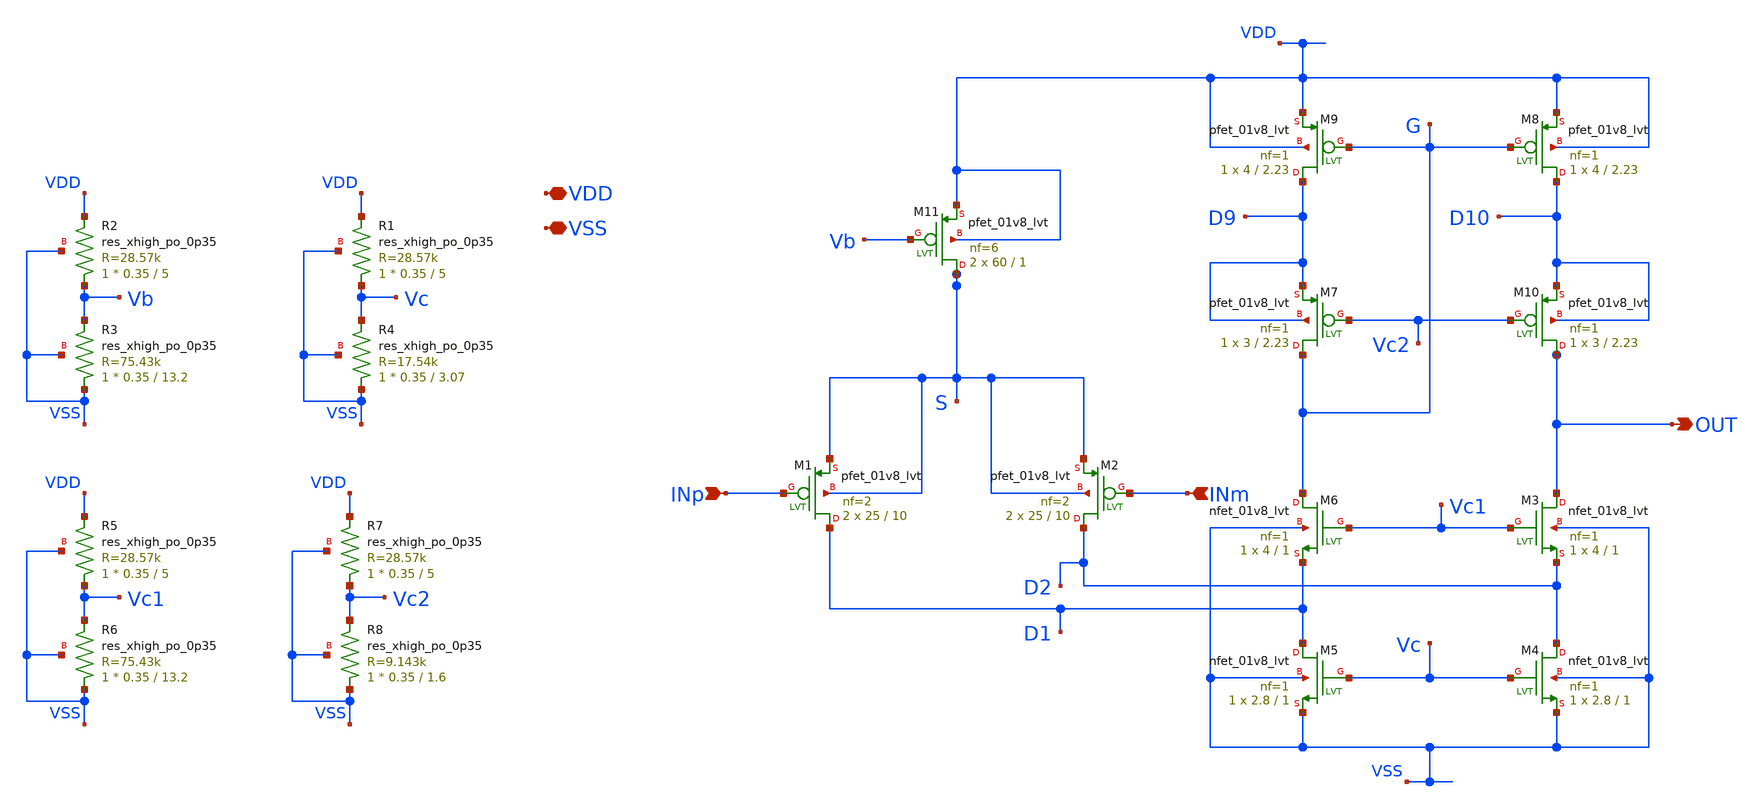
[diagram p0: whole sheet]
** sch_path: tt_um_NE567Mixer28/xschem/OFC.sch
**.subckt OFC VDD VSS INp INm OUT
*.iopin VDD
*.iopin VSS
*.ipin INp
*.ipin INm
*.opin OUT
XM11 S Vb VDD VDD sky130_fd_pr__pfet_01v8_lvt L=1 W=60 nf=6 ad='int((nf+1)/2) * W/nf * 0.29' as='int((nf+2)/2) * W/nf * 0.29'
+ pd='2*int((nf+1)/2) * (W/nf + 0.29)' ps='2*int((nf+2)/2) * (W/nf + 0.29)' nrd='0.29 / W' nrs='0.29 / W'
+ sa=0 sb=0 sd=0 mult=2 m=2
XM1 D1 INp S S sky130_fd_pr__pfet_01v8_lvt L=10 W=25 nf=2 ad='int((nf+1)/2) * W/nf * 0.29' as='int((nf+2)/2) * W/nf * 0.29'
+ pd='2*int((nf+1)/2) * (W/nf + 0.29)' ps='2*int((nf+2)/2) * (W/nf + 0.29)' nrd='0.29 / W' nrs='0.29 / W'
+ sa=0 sb=0 sd=0 mult=2 m=2
XM2 D2 INm S S sky130_fd_pr__pfet_01v8_lvt L=10 W=25 nf=2 ad='int((nf+1)/2) * W/nf * 0.29' as='int((nf+2)/2) * W/nf * 0.29'
+ pd='2*int((nf+1)/2) * (W/nf + 0.29)' ps='2*int((nf+2)/2) * (W/nf + 0.29)' nrd='0.29 / W' nrs='0.29 / W'
+ sa=0 sb=0 sd=0 mult=2 m=2
XM3 OUT Vc1 D2 VSS sky130_fd_pr__nfet_01v8_lvt L=1 W=4 nf=1 ad='int((nf+1)/2) * W/nf * 0.29' as='int((nf+2)/2) * W/nf * 0.29'
+ pd='2*int((nf+1)/2) * (W/nf + 0.29)' ps='2*int((nf+2)/2) * (W/nf + 0.29)' nrd='0.29 / W' nrs='0.29 / W'
+ sa=0 sb=0 sd=0 mult=1 m=1
XM4 D2 Vc VSS VSS sky130_fd_pr__nfet_01v8_lvt L=1 W=2.8 nf=1 ad='int((nf+1)/2) * W/nf * 0.29' as='int((nf+2)/2) * W/nf * 0.29'
+ pd='2*int((nf+1)/2) * (W/nf + 0.29)' ps='2*int((nf+2)/2) * (W/nf + 0.29)' nrd='0.29 / W' nrs='0.29 / W'
+ sa=0 sb=0 sd=0 mult=1 m=1
XM5 D1 Vc VSS VSS sky130_fd_pr__nfet_01v8_lvt L=1 W=2.8 nf=1 ad='int((nf+1)/2) * W/nf * 0.29' as='int((nf+2)/2) * W/nf * 0.29'
+ pd='2*int((nf+1)/2) * (W/nf + 0.29)' ps='2*int((nf+2)/2) * (W/nf + 0.29)' nrd='0.29 / W' nrs='0.29 / W'
+ sa=0 sb=0 sd=0 mult=1 m=1
XM6 G Vc1 D1 VSS sky130_fd_pr__nfet_01v8_lvt L=1 W=4 nf=1 ad='int((nf+1)/2) * W/nf * 0.29' as='int((nf+2)/2) * W/nf * 0.29'
+ pd='2*int((nf+1)/2) * (W/nf + 0.29)' ps='2*int((nf+2)/2) * (W/nf + 0.29)' nrd='0.29 / W' nrs='0.29 / W'
+ sa=0 sb=0 sd=0 mult=1 m=1
XM7 G Vc2 D9 D9 sky130_fd_pr__pfet_01v8_lvt L=2.23 W=3 nf=1 ad='int((nf+1)/2) * W/nf * 0.29' as='int((nf+2)/2) * W/nf * 0.29'
+ pd='2*int((nf+1)/2) * (W/nf + 0.29)' ps='2*int((nf+2)/2) * (W/nf + 0.29)' nrd='0.29 / W' nrs='0.29 / W'
+ sa=0 sb=0 sd=0 mult=1 m=1
XM9 D9 G VDD VDD sky130_fd_pr__pfet_01v8_lvt L=2.23 W=4 nf=1 ad='int((nf+1)/2) * W/nf * 0.29' as='int((nf+2)/2) * W/nf * 0.29'
+ pd='2*int((nf+1)/2) * (W/nf + 0.29)' ps='2*int((nf+2)/2) * (W/nf + 0.29)' nrd='0.29 / W' nrs='0.29 / W'
+ sa=0 sb=0 sd=0 mult=1 m=1
XM8 D10 G VDD VDD sky130_fd_pr__pfet_01v8_lvt L=2.23 W=4 nf=1 ad='int((nf+1)/2) * W/nf * 0.29' as='int((nf+2)/2) * W/nf * 0.29'
+ pd='2*int((nf+1)/2) * (W/nf + 0.29)' ps='2*int((nf+2)/2) * (W/nf + 0.29)' nrd='0.29 / W' nrs='0.29 / W'
+ sa=0 sb=0 sd=0 mult=1 m=1
XM10 OUT Vc2 D10 D10 sky130_fd_pr__pfet_01v8_lvt L=2.23 W=3 nf=1 ad='int((nf+1)/2) * W/nf * 0.29' as='int((nf+2)/2) * W/nf * 0.29'
+ pd='2*int((nf+1)/2) * (W/nf + 0.29)' ps='2*int((nf+2)/2) * (W/nf + 0.29)' nrd='0.29 / W' nrs='0.29 / W'
+ sa=0 sb=0 sd=0 mult=1 m=1
XR2 Vb VDD VSS sky130_fd_pr__res_xhigh_po_0p35 L=5 mult=1 m=1
XR3 VSS Vb VSS sky130_fd_pr__res_xhigh_po_0p35 L=13.2 mult=1 m=1
XR1 Vc VDD VSS sky130_fd_pr__res_xhigh_po_0p35 L=5 mult=1 m=1
XR4 VSS Vc VSS sky130_fd_pr__res_xhigh_po_0p35 L=3.07 mult=1 m=1
XR5 Vc1 VDD VSS sky130_fd_pr__res_xhigh_po_0p35 L=5 mult=1 m=1
XR6 VSS Vc1 VSS sky130_fd_pr__res_xhigh_po_0p35 L=13.2 mult=1 m=1
XR7 Vc2 VDD VSS sky130_fd_pr__res_xhigh_po_0p35 L=5 mult=1 m=1
XR8 VSS Vc2 VSS sky130_fd_pr__res_xhigh_po_0p35 L=1.6 mult=1 m=1
**.ends
.end
